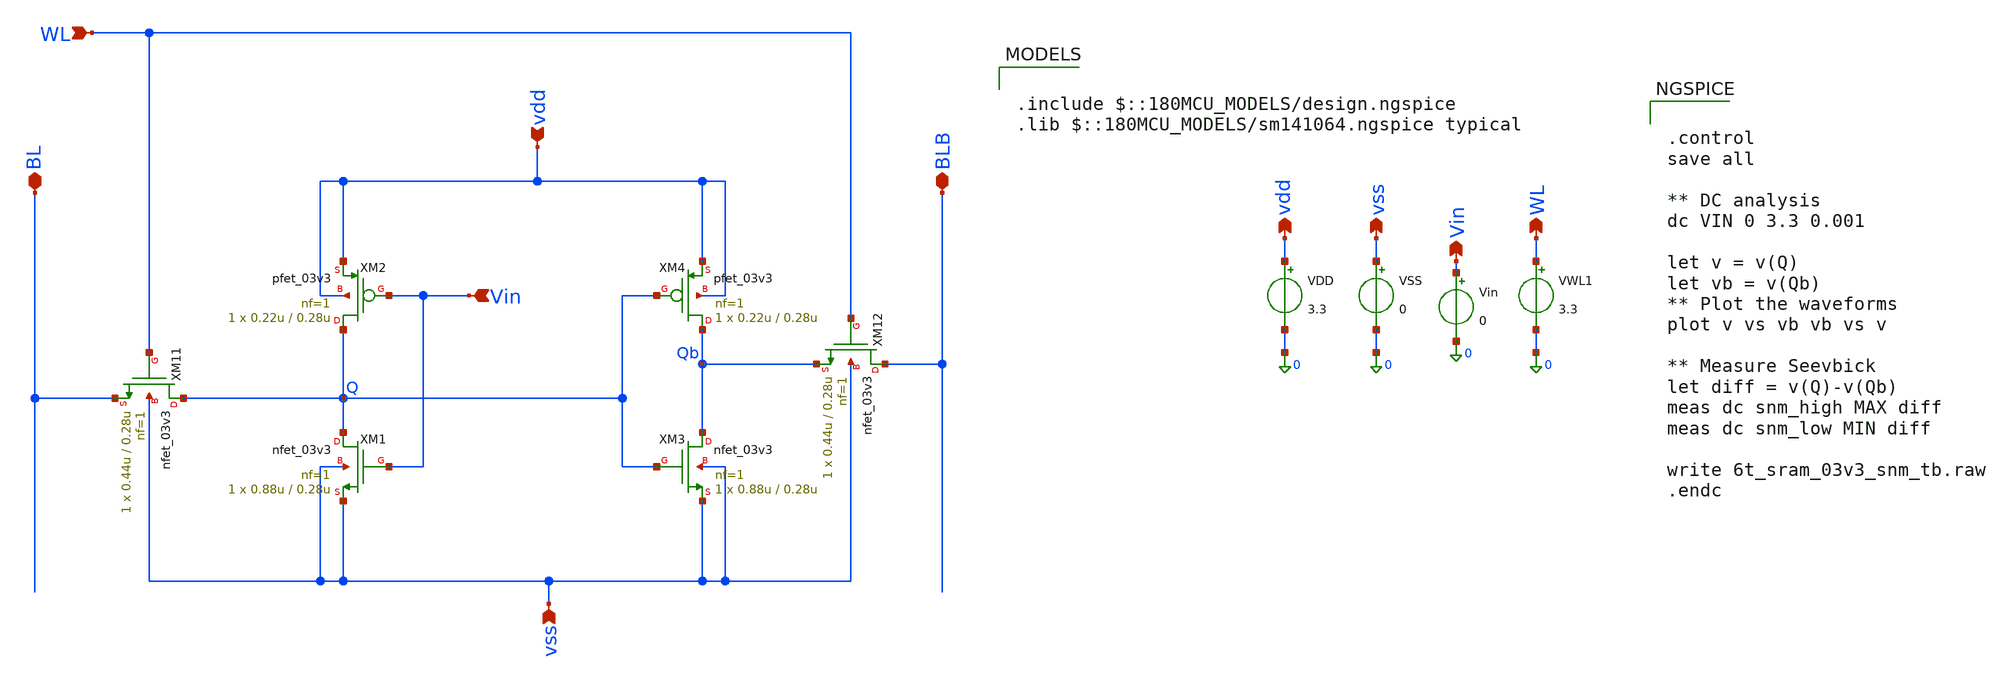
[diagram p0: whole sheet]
** sch_path: sim/analog/6t_sram_03v3_snm_tb.sch
**.subckt 6t_sram_03v3_snm_tb vdd vss vdd vss Vin Vin BL WL BLB WL
*.ipin vdd
*.ipin vss
*.opin vdd
*.opin vss
*.opin Vin
*.ipin Vin
*.iopin BL
*.ipin WL
*.iopin BLB
*.opin WL
XM1 Q Vin vss vss nfet_03v3 L=0.28u W=0.88u nf=1 ad='int((nf+1)/2) * W/nf * 0.18u' as='int((nf+2)/2) * W/nf * 0.18u'
+ pd='2*int((nf+1)/2) * (W/nf + 0.18u)' ps='2*int((nf+2)/2) * (W/nf + 0.18u)' nrd='0.18u / W' nrs='0.18u / W'
+ sa=0 sb=0 sd=0 m=1
XM2 Q Vin vdd vdd pfet_03v3 L=0.28u W=0.22u nf=1 ad='int((nf+1)/2) * W/nf * 0.18u' as='int((nf+2)/2) * W/nf * 0.18u'
+ pd='2*int((nf+1)/2) * (W/nf + 0.18u)' ps='2*int((nf+2)/2) * (W/nf + 0.18u)' nrd='0.18u / W' nrs='0.18u / W'
+ sa=0 sb=0 sd=0 m=1
XM3 Qb Q vss vss nfet_03v3 L=0.28u W=0.88u nf=1 ad='int((nf+1)/2) * W/nf * 0.18u' as='int((nf+2)/2) * W/nf * 0.18u'
+ pd='2*int((nf+1)/2) * (W/nf + 0.18u)' ps='2*int((nf+2)/2) * (W/nf + 0.18u)' nrd='0.18u / W' nrs='0.18u / W'
+ sa=0 sb=0 sd=0 m=1
XM4 Qb Q vdd vdd pfet_03v3 L=0.28u W=0.22u nf=1 ad='int((nf+1)/2) * W/nf * 0.18u' as='int((nf+2)/2) * W/nf * 0.18u'
+ pd='2*int((nf+1)/2) * (W/nf + 0.18u)' ps='2*int((nf+2)/2) * (W/nf + 0.18u)' nrd='0.18u / W' nrs='0.18u / W'
+ sa=0 sb=0 sd=0 m=1
VDD vdd 0 3.3
VSS vss 0 0
Vin Vin 0 0
XM11 Q WL BL vss nfet_03v3 L=0.28u W=0.44u nf=1 ad='int((nf+1)/2) * W/nf * 0.18u' as='int((nf+2)/2) * W/nf * 0.18u'
+ pd='2*int((nf+1)/2) * (W/nf + 0.18u)' ps='2*int((nf+2)/2) * (W/nf + 0.18u)' nrd='0.18u / W' nrs='0.18u / W'
+ sa=0 sb=0 sd=0 m=1
XM12 BLB WL Qb vss nfet_03v3 L=0.28u W=0.44u nf=1 ad='int((nf+1)/2) * W/nf * 0.18u' as='int((nf+2)/2) * W/nf * 0.18u'
+ pd='2*int((nf+1)/2) * (W/nf + 0.18u)' ps='2*int((nf+2)/2) * (W/nf + 0.18u)' nrd='0.18u / W' nrs='0.18u / W'
+ sa=0 sb=0 sd=0 m=1
VWL1 WL 0 3.3
**** begin user architecture code

.include $::180MCU_MODELS/design.ngspice
.lib $::180MCU_MODELS/sm141064.ngspice typical



.control
save all

** DC analysis
dc VIN 0 3.3 0.001

let v = v(Q)
let vb = v(Qb)
** Plot the waveforms
plot v vs vb vb vs v

** Measure Seevbick
let diff = v(Q)-v(Qb)
meas dc snm_high MAX diff
meas dc snm_low MIN diff

write 6t_sram_03v3_snm_tb.raw
.endc



**** end user architecture code
**.ends
.end
